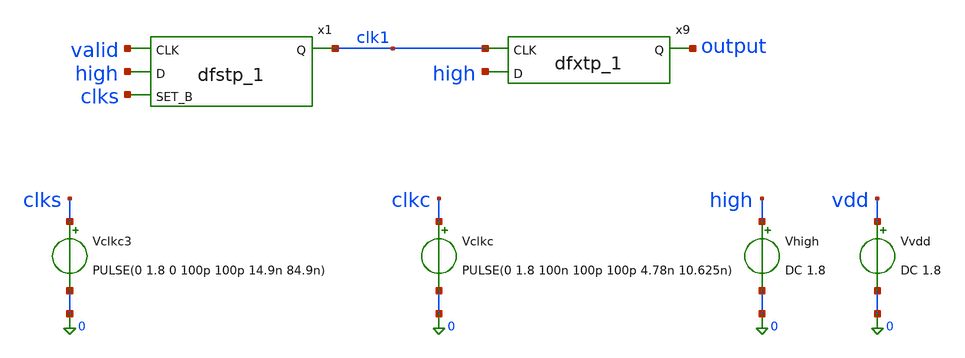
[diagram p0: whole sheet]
** sch_path: xschem/sar-adc_tb/sarblock_tb.sch
**.subckt sarblock_tb
x1 valid high clks 0 0 vdd vdd clk1 sky130_fd_sc_hd__dfstp_1
x9 clk1 high 0 0 vdd vdd output sky130_fd_sc_hd__dfxtp_1
Vclkc3 clks 0 PULSE(0 1.8 0 100p 100p 14.9n 84.9n)
Vclkc clkc 0 PULSE(0 1.8 100n 100p 100p 4.78n 10.625n)
Vhigh high 0 DC 1.8
Vvdd vdd 0 DC 1.8
**.ends
.end
